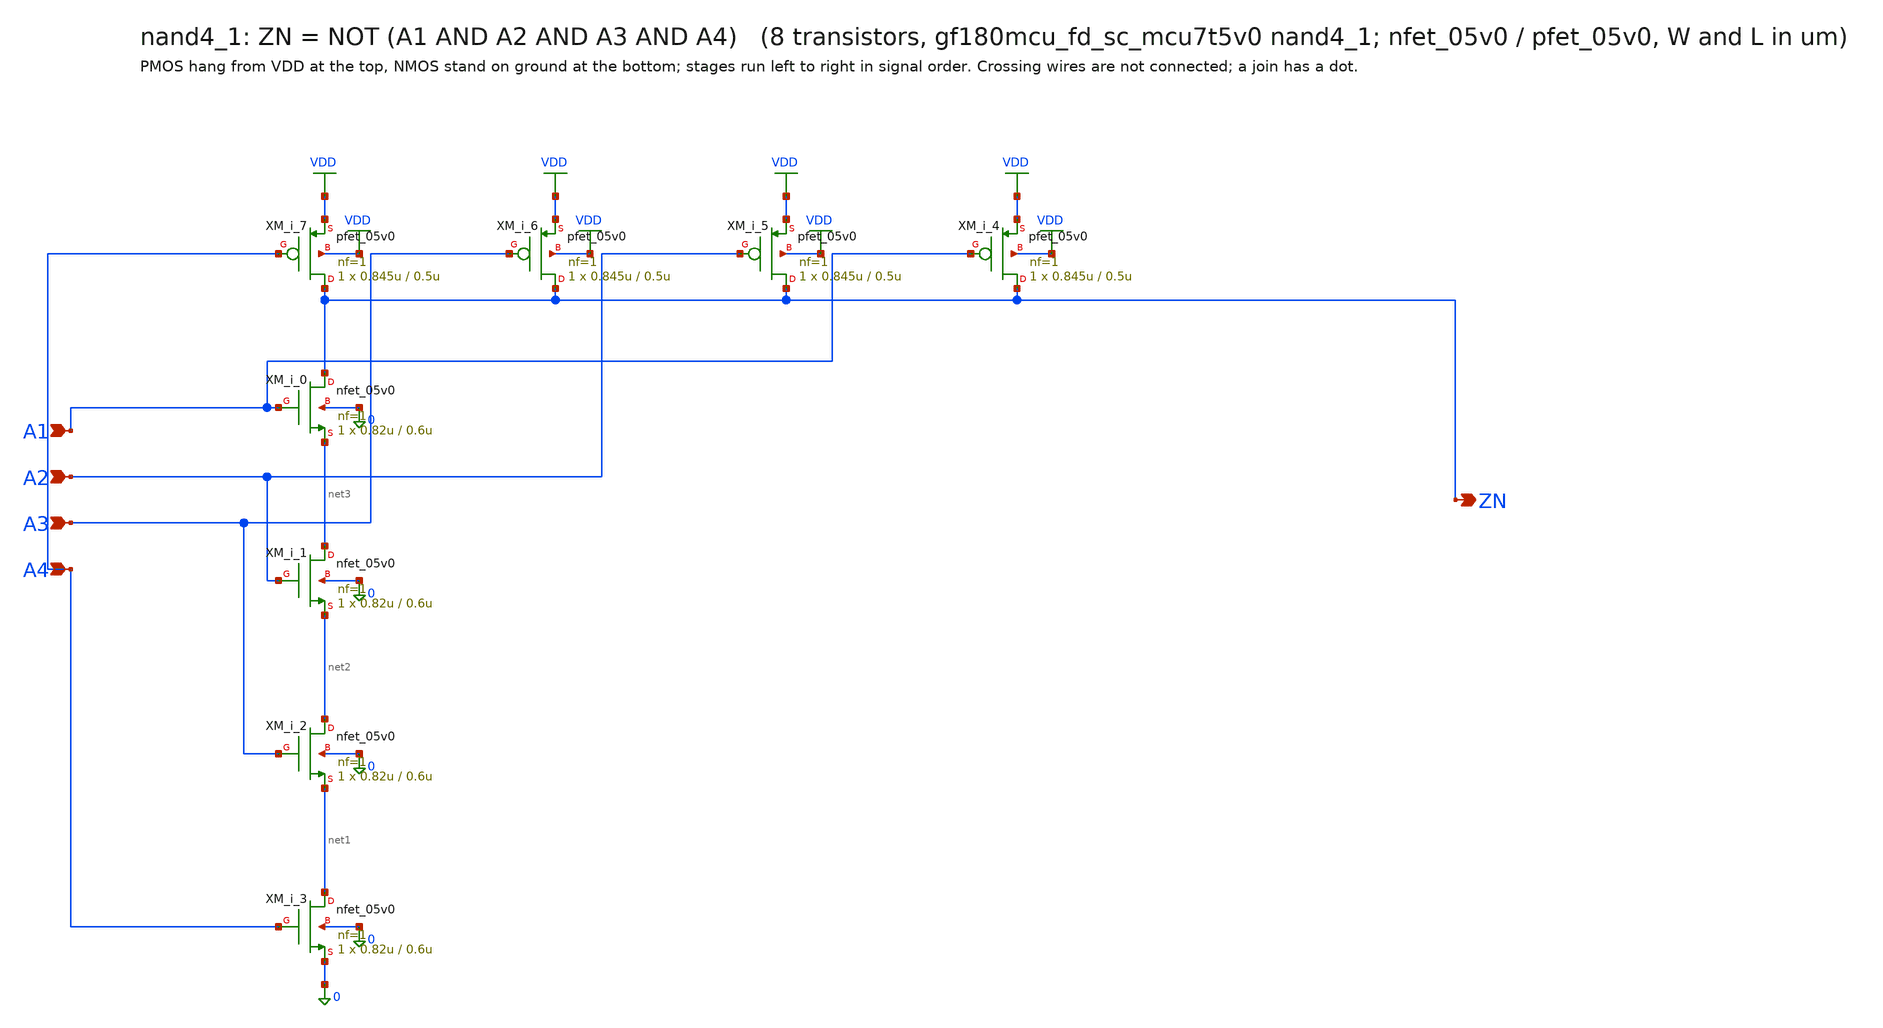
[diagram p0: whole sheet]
** sch_path: xschem/cells_tx/nand4_1.sch
**.subckt nand4_1 A1 A2 A3 A4 ZN
*.ipin A1
*.ipin A2
*.ipin A3
*.ipin A4
*.opin ZN
XM_i_3 net1 A4 0 0 nfet_05v0 L=0.6u W=0.82u nf=1 ad=4.1e-13 as=4.1e-13 pd=2.64e-06 ps=2.64e-06 nrd=0
+ nrs=0 sa=0 sb=0 sd=0 m=1
XM_i_2 net2 A3 net1 0 nfet_05v0 L=0.6u W=0.82u nf=1 ad=4.1e-13 as=4.1e-13 pd=2.64e-06 ps=2.64e-06
+ nrd=0 nrs=0 sa=0 sb=0 sd=0 m=1
XM_i_1 net3 A2 net2 0 nfet_05v0 L=0.6u W=0.82u nf=1 ad=4.1e-13 as=4.1e-13 pd=2.64e-06 ps=2.64e-06
+ nrd=0 nrs=0 sa=0 sb=0 sd=0 m=1
XM_i_0 ZN A1 net3 0 nfet_05v0 L=0.6u W=0.82u nf=1 ad=4.1e-13 as=4.1e-13 pd=2.64e-06 ps=2.64e-06
+ nrd=0 nrs=0 sa=0 sb=0 sd=0 m=1
XM_i_7 ZN A4 VDD VDD pfet_05v0 L=0.5u W=0.845u nf=1 ad=4.225e-13 as=4.225e-13 pd=2.69e-06
+ ps=2.69e-06 nrd=0 nrs=0 sa=0 sb=0 sd=0 m=1
XM_i_6 ZN A3 VDD VDD pfet_05v0 L=0.5u W=0.845u nf=1 ad=4.225e-13 as=4.225e-13 pd=2.69e-06
+ ps=2.69e-06 nrd=0 nrs=0 sa=0 sb=0 sd=0 m=1
XM_i_5 ZN A2 VDD VDD pfet_05v0 L=0.5u W=0.845u nf=1 ad=4.225e-13 as=4.225e-13 pd=2.69e-06
+ ps=2.69e-06 nrd=0 nrs=0 sa=0 sb=0 sd=0 m=1
XM_i_4 ZN A1 VDD VDD pfet_05v0 L=0.5u W=0.845u nf=1 ad=4.225e-13 as=4.225e-13 pd=2.69e-06
+ ps=2.69e-06 nrd=0 nrs=0 sa=0 sb=0 sd=0 m=1
**.ends
.GLOBAL VDD
.end
